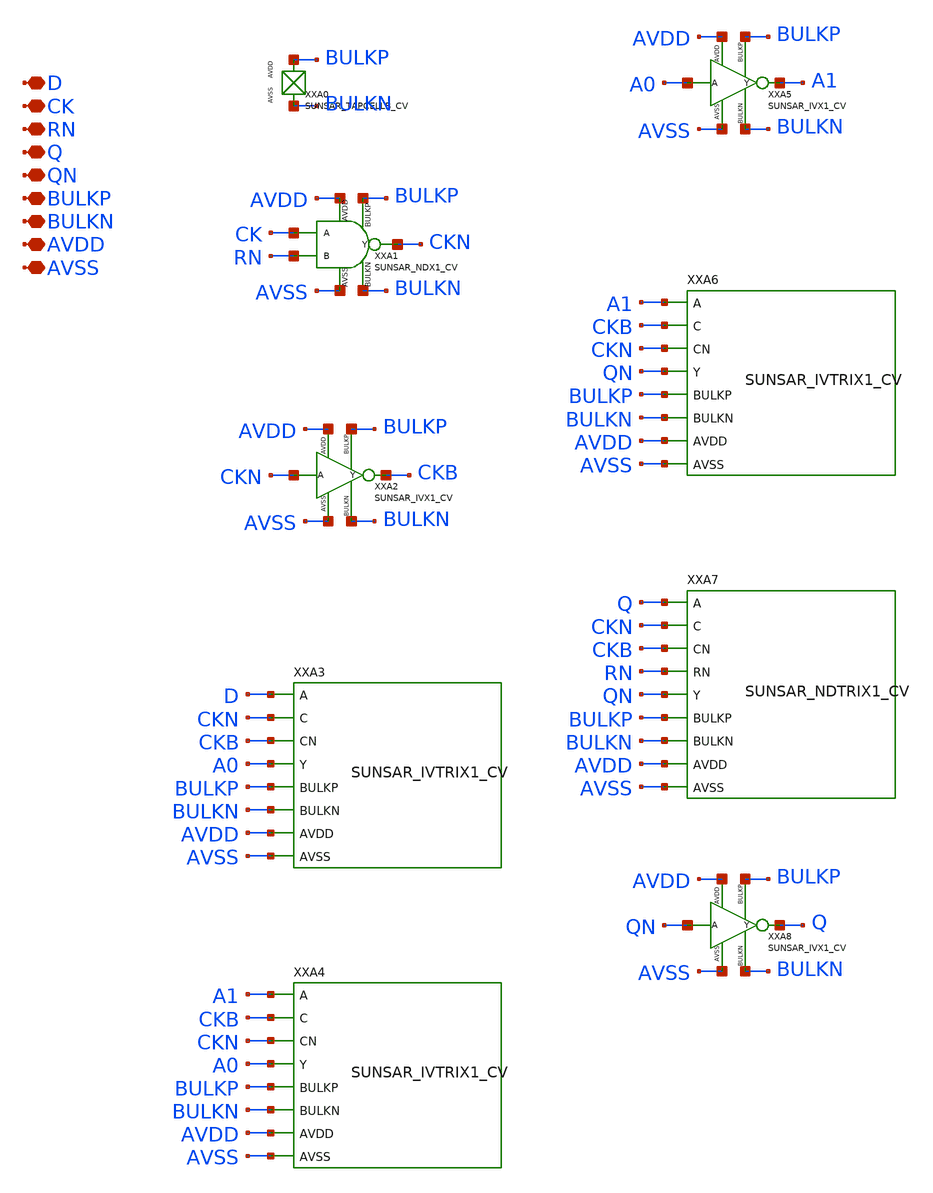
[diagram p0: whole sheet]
** sch_path: design/SUN_SAR9B_SKY130NM/SUNSAR_DFRNQNX1_CV.sch
**.subckt SUNSAR_DFRNQNX1_CV D CK RN Q QN BULKP BULKN AVDD AVSS
*.iopin D
*.iopin CK
*.iopin RN
*.iopin Q
*.iopin QN
*.iopin BULKP
*.iopin BULKN
*.iopin AVDD
*.iopin AVSS
XXA0 BULKP BULKN SUNSAR_TAPCELLB_CV
XXA1 CK RN CKN BULKP BULKN AVDD AVSS SUNSAR_NDX1_CV
XXA2 CKN CKB BULKP BULKN AVDD AVSS SUNSAR_IVX1_CV
XXA3 D CKN CKB A0 BULKP BULKN AVDD AVSS SUNSAR_IVTRIX1_CV
XXA4 A1 CKB CKN A0 BULKP BULKN AVDD AVSS SUNSAR_IVTRIX1_CV
XXA5 A0 A1 BULKP BULKN AVDD AVSS SUNSAR_IVX1_CV
XXA6 A1 CKB CKN QN BULKP BULKN AVDD AVSS SUNSAR_IVTRIX1_CV
XXA7 Q CKN CKB RN QN BULKP BULKN AVDD AVSS SUNSAR_NDTRIX1_CV
XXA8 QN Q BULKP BULKN AVDD AVSS SUNSAR_IVX1_CV
**.ends
.end
